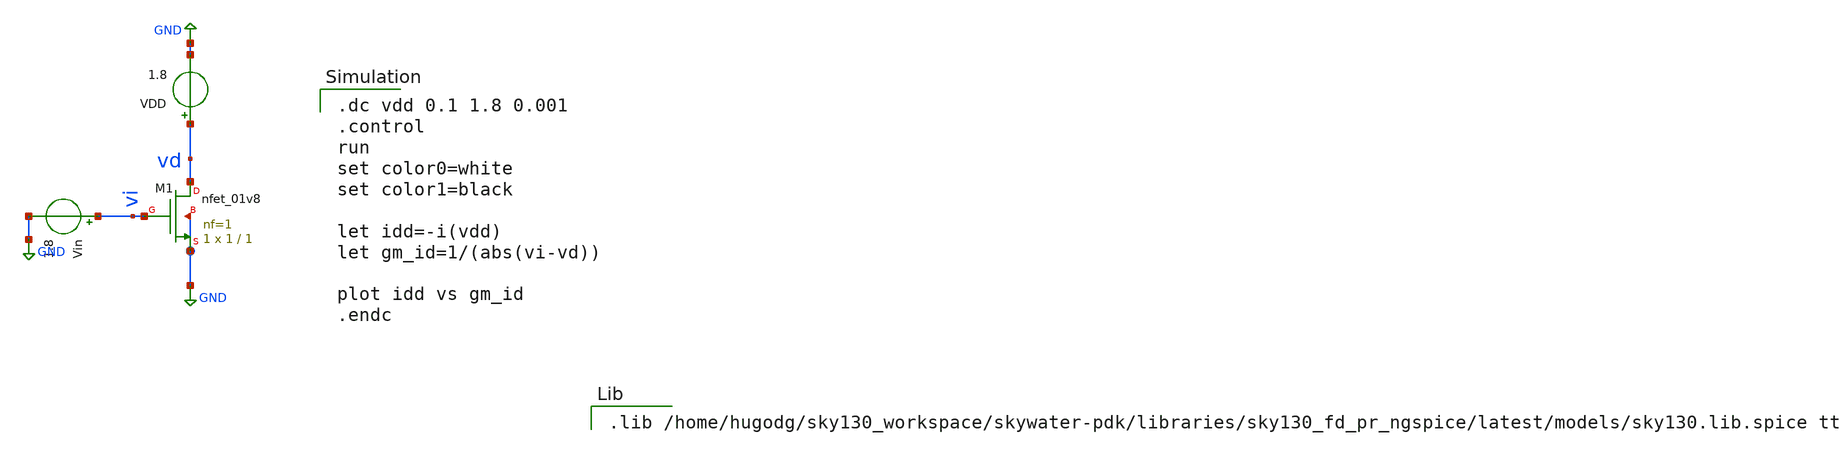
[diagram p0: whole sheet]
** sch_path: mag/sensor/xschem/gm-id_1v8.sch
**.subckt gm-id_1v8
VDD vd GND 1.8
Vin vi GND 1.8
XM1 vd vi GND GND sky130_fd_pr__nfet_01v8 L=1 W=1 nf=1 ad='int((nf+1)/2) * W/nf * 0.29' as='int((nf+2)/2) * W/nf * 0.29'
+ pd='2*int((nf+1)/2) * (W/nf + 0.29)' ps='2*int((nf+2)/2) * (W/nf + 0.29)' nrd='0.29 / W' nrs='0.29 / W'
+ sa=0 sb=0 sd=0 mult=1 m=1
**** begin user architecture code

.dc vdd 0.1 1.8 0.001
.control
run
set color0=white
set color1=black

let idd=-i(vdd)
let gm_id=1/(abs(vi-vd))

plot idd vs gm_id
.endc



.lib /home/hugodg/sky130_workspace/skywater-pdk/libraries/sky130_fd_pr_ngspice/latest/models/sky130.lib.spice tt

**** end user architecture code
**.ends
.GLOBAL GND
.end
